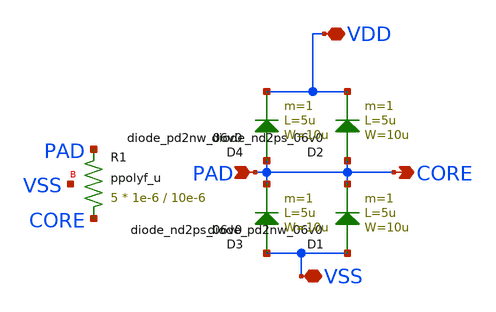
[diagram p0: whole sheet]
** sch_path: FINAL/XSCHEM_v2/ESD_CDM2.sch
**.subckt ESD_CDM2 PAD CORE VDD VSS
*.ipin PAD
*.opin CORE
*.iopin VDD
*.iopin VSS
D1 VSS PAD diode_pd2nw_06v0 area='10u * 5u ' pj='2*10u + 2*5u ' m=1
D2 PAD VDD diode_nd2ps_06v0 area='10u * 5u ' pj='2*10u + 2*5u ' m=1
D3 VSS PAD diode_nd2ps_06v0 area='10u * 5u ' pj='2*10u + 2*5u ' m=1
D4 PAD VDD diode_pd2nw_06v0 area='10u * 5u ' pj='2*10u + 2*5u ' m=1
XR1 CORE PAD VSS ppolyf_u r_width=1e-6 r_length=10e-6 m=5
**.ends
.end
